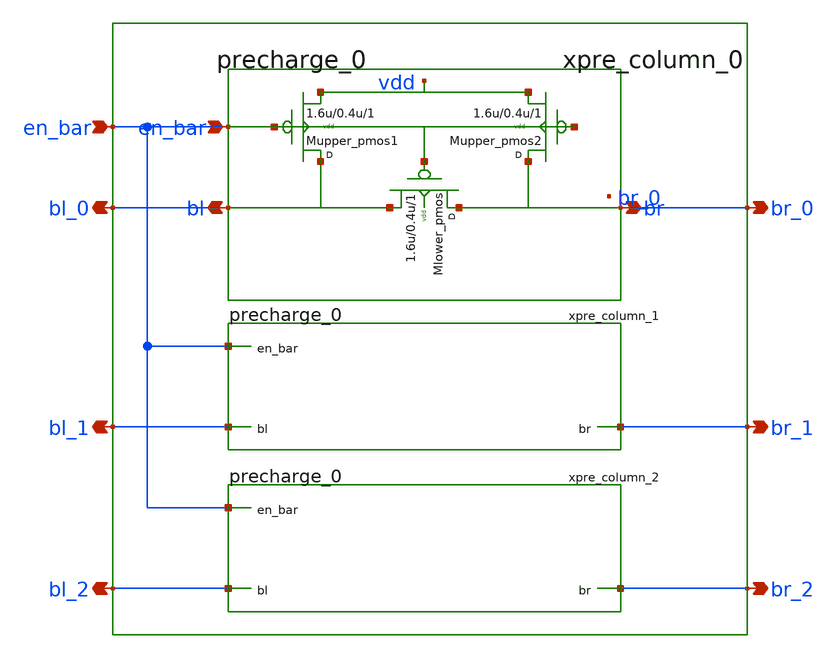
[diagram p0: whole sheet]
** sch_path: sram_2_16_scn4m/precharge_array.sch
**.subckt precharge_array bl_0 br_0 bl_1 br_1 bl_2 br_2 en_bar
*.opin bl_0
*.opin br_0
*.opin bl_1
*.opin br_1
*.opin bl_2
*.opin br_2
*.ipin en_bar
xpre_column_1 bl_1 br_1 en_bar vdd precharge_0
xpre_column_2 bl_2 br_2 en_bar vdd precharge_0
xpre_column_0 bl_0 br_0 en_bar vdd precharge_0
**.ends
.end
